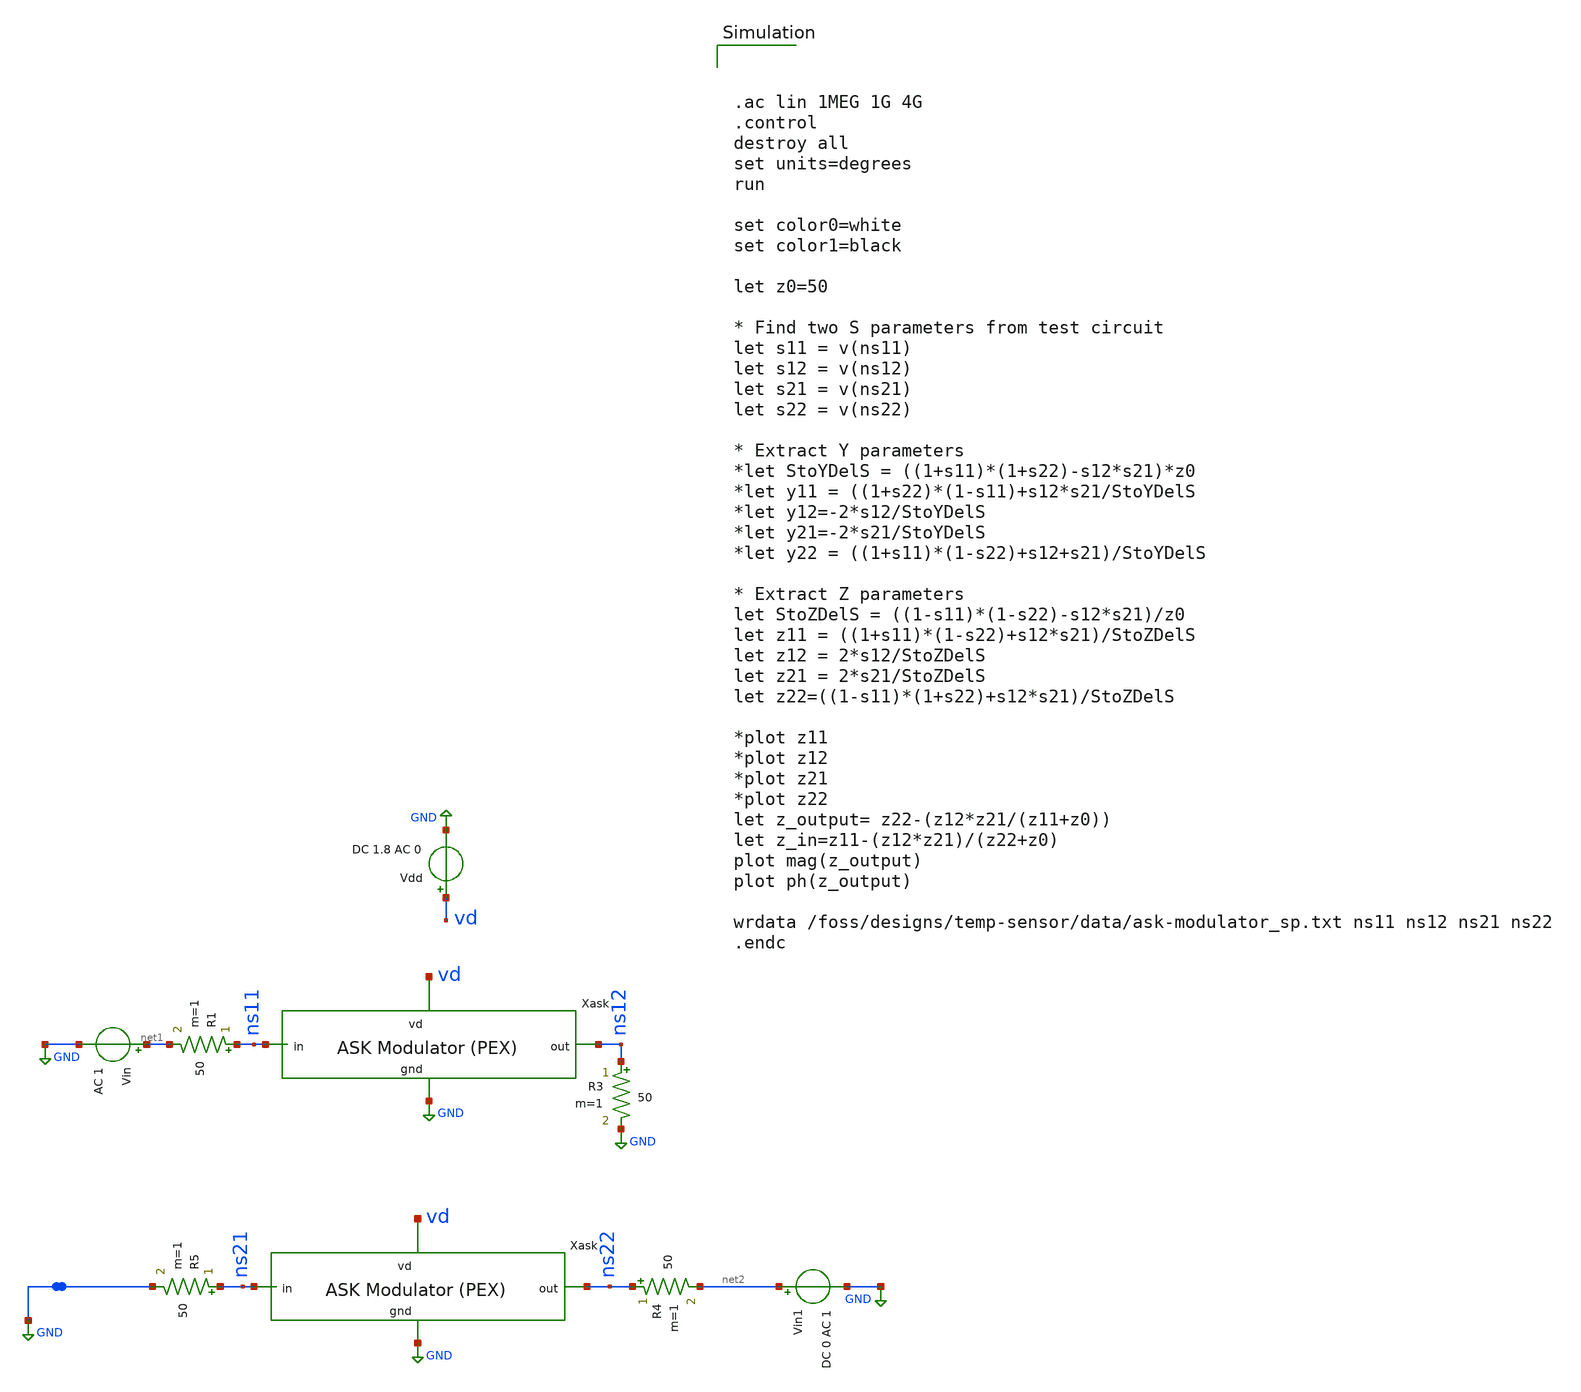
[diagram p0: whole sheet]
** sch_path: ask_modulator/xschem/ask-modulator_tb-sp.sch
**.subckt ask-modulator_tb-sp
Vdd vd GND DC 1.8 AC 0
Vin net1 GND AC 1
Vin1 net2 GND DC 0 AC 1
R1 ns11 net1 50 m=1
R3 ns12 GND 50 m=1
R4 ns22 net2 50 m=1
R5 ns21 GND 50 m=1
x1 vd ns12 ns11 GND ask-modulator-pex
x2 vd ns22 ns21 GND ask-modulator-pex
**** begin user architecture code



.ac lin 1MEG 1G 4G
.control
destroy all
set units=degrees
run

set color0=white
set color1=black

let z0=50

* Find two S parameters from test circuit
let s11 = v(ns11)
let s12 = v(ns12)
let s21 = v(ns21)
let s22 = v(ns22)

* Extract Y parameters
*let StoYDelS = ((1+s11)*(1+s22)-s12*s21)*z0
*let y11 = ((1+s22)*(1-s11)+s12*s21/StoYDelS
*let y12=-2*s12/StoYDelS
*let y21=-2*s21/StoYDelS
*let y22 = ((1+s11)*(1-s22)+s12+s21)/StoYDelS

* Extract Z parameters
let StoZDelS = ((1-s11)*(1-s22)-s12*s21)/z0
let z11 = ((1+s11)*(1-s22)+s12*s21)/StoZDelS
let z12 = 2*s12/StoZDelS
let z21 = 2*s21/StoZDelS
let z22=((1-s11)*(1+s22)+s12*s21)/StoZDelS

*plot z11
*plot z12
*plot z21
*plot z22
let z_output= z22-(z12*z21/(z11+z0))
let z_in=z11-(z12*z21)/(z22+z0)
plot mag(z_output)
plot ph(z_output)

wrdata /foss/designs/temp-sensor/data/ask-modulator_sp.txt ns11 ns12 ns21 ns22
.endc

 .lib $::SKYWATER_MODELS/sky130.lib.spice tt
.include $::SKYWATER_STDCELLS/sky130_fd_sc_hd.spice

**** end user architecture code
**.ends
.GLOBAL GND
.end
